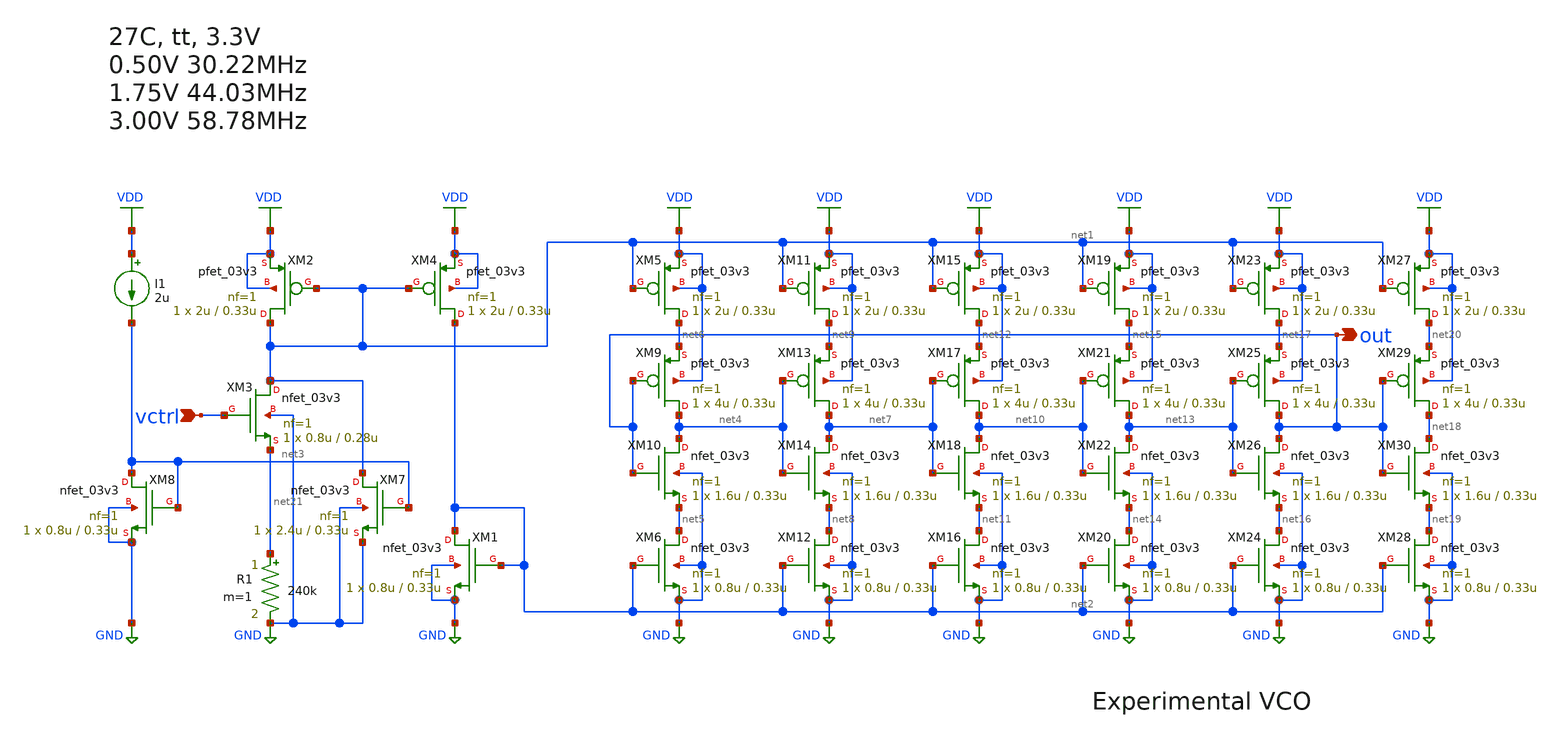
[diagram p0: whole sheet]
** sch_path: PLL/xschem/vco.sch
**.subckt vco vctrl out
*.ipin vctrl
*.opin out
XM2 net1 net1 VDD VDD pfet_03v3 L=0.33u W=2u nf=1 ad='int((nf+1)/2) * W/nf * 0.18u' as='int((nf+2)/2) * W/nf * 0.18u'
+ pd='2*int((nf+1)/2) * (W/nf + 0.18u)' ps='2*int((nf+2)/2) * (W/nf + 0.18u)' nrd='0.18u / W' nrs='0.18u / W'
+ sa=0 sb=0 sd=0 m=1
XM4 net2 net1 VDD VDD pfet_03v3 L=0.33u W=2u nf=1 ad='int((nf+1)/2) * W/nf * 0.18u' as='int((nf+2)/2) * W/nf * 0.18u'
+ pd='2*int((nf+1)/2) * (W/nf + 0.18u)' ps='2*int((nf+2)/2) * (W/nf + 0.18u)' nrd='0.18u / W' nrs='0.18u / W'
+ sa=0 sb=0 sd=0 m=1
XM1 net2 net2 GND GND nfet_03v3 L=0.33u W=0.8u nf=1 ad='int((nf+1)/2) * W/nf * 0.18u' as='int((nf+2)/2) * W/nf * 0.18u'
+ pd='2*int((nf+1)/2) * (W/nf + 0.18u)' ps='2*int((nf+2)/2) * (W/nf + 0.18u)' nrd='0.18u / W' nrs='0.18u / W'
+ sa=0 sb=0 sd=0 m=1
XM5 net6 net1 VDD VDD pfet_03v3 L=0.33u W=2u nf=1 ad='int((nf+1)/2) * W/nf * 0.18u' as='int((nf+2)/2) * W/nf * 0.18u'
+ pd='2*int((nf+1)/2) * (W/nf + 0.18u)' ps='2*int((nf+2)/2) * (W/nf + 0.18u)' nrd='0.18u / W' nrs='0.18u / W'
+ sa=0 sb=0 sd=0 m=1
XM6 net5 net2 GND GND nfet_03v3 L=0.33u W=0.8u nf=1 ad='int((nf+1)/2) * W/nf * 0.18u' as='int((nf+2)/2) * W/nf * 0.18u'
+ pd='2*int((nf+1)/2) * (W/nf + 0.18u)' ps='2*int((nf+2)/2) * (W/nf + 0.18u)' nrd='0.18u / W' nrs='0.18u / W'
+ sa=0 sb=0 sd=0 m=1
I1 VDD net3 2u
XM8 net3 net3 GND GND nfet_03v3 L=0.33u W=0.8u nf=1 ad='int((nf+1)/2) * W/nf * 0.18u' as='int((nf+2)/2) * W/nf * 0.18u'
+ pd='2*int((nf+1)/2) * (W/nf + 0.18u)' ps='2*int((nf+2)/2) * (W/nf + 0.18u)' nrd='0.18u / W' nrs='0.18u / W'
+ sa=0 sb=0 sd=0 m=1
R1 net21 GND 240k m=1
XM3 net1 vctrl net21 GND nfet_03v3 L=0.28u W=0.8u nf=1 ad='int((nf+1)/2) * W/nf * 0.18u' as='int((nf+2)/2) * W/nf * 0.18u'
+ pd='2*int((nf+1)/2) * (W/nf + 0.18u)' ps='2*int((nf+2)/2) * (W/nf + 0.18u)' nrd='0.18u / W' nrs='0.18u / W'
+ sa=0 sb=0 sd=0 m=1
XM7 net1 net3 GND GND nfet_03v3 L=0.33u W=2.4u nf=1 ad='int((nf+1)/2) * W/nf * 0.18u' as='int((nf+2)/2) * W/nf * 0.18u'
+ pd='2*int((nf+1)/2) * (W/nf + 0.18u)' ps='2*int((nf+2)/2) * (W/nf + 0.18u)' nrd='0.18u / W' nrs='0.18u / W'
+ sa=0 sb=0 sd=0 m=1
XM9 net4 out net6 VDD pfet_03v3 L=0.33u W=4u nf=1 ad='int((nf+1)/2) * W/nf * 0.18u' as='int((nf+2)/2) * W/nf * 0.18u'
+ pd='2*int((nf+1)/2) * (W/nf + 0.18u)' ps='2*int((nf+2)/2) * (W/nf + 0.18u)' nrd='0.18u / W' nrs='0.18u / W'
+ sa=0 sb=0 sd=0 m=1
XM10 net4 out net5 GND nfet_03v3 L=0.33u W=1.6u nf=1 ad='int((nf+1)/2) * W/nf * 0.18u' as='int((nf+2)/2) * W/nf * 0.18u'
+ pd='2*int((nf+1)/2) * (W/nf + 0.18u)' ps='2*int((nf+2)/2) * (W/nf + 0.18u)' nrd='0.18u / W' nrs='0.18u / W'
+ sa=0 sb=0 sd=0 m=1
XM11 net9 net1 VDD VDD pfet_03v3 L=0.33u W=2u nf=1 ad='int((nf+1)/2) * W/nf * 0.18u' as='int((nf+2)/2) * W/nf * 0.18u'
+ pd='2*int((nf+1)/2) * (W/nf + 0.18u)' ps='2*int((nf+2)/2) * (W/nf + 0.18u)' nrd='0.18u / W' nrs='0.18u / W'
+ sa=0 sb=0 sd=0 m=1
XM12 net8 net2 GND GND nfet_03v3 L=0.33u W=0.8u nf=1 ad='int((nf+1)/2) * W/nf * 0.18u' as='int((nf+2)/2) * W/nf * 0.18u'
+ pd='2*int((nf+1)/2) * (W/nf + 0.18u)' ps='2*int((nf+2)/2) * (W/nf + 0.18u)' nrd='0.18u / W' nrs='0.18u / W'
+ sa=0 sb=0 sd=0 m=1
XM13 net7 net4 net9 VDD pfet_03v3 L=0.33u W=4u nf=1 ad='int((nf+1)/2) * W/nf * 0.18u' as='int((nf+2)/2) * W/nf * 0.18u'
+ pd='2*int((nf+1)/2) * (W/nf + 0.18u)' ps='2*int((nf+2)/2) * (W/nf + 0.18u)' nrd='0.18u / W' nrs='0.18u / W'
+ sa=0 sb=0 sd=0 m=1
XM14 net7 net4 net8 GND nfet_03v3 L=0.33u W=1.6u nf=1 ad='int((nf+1)/2) * W/nf * 0.18u' as='int((nf+2)/2) * W/nf * 0.18u'
+ pd='2*int((nf+1)/2) * (W/nf + 0.18u)' ps='2*int((nf+2)/2) * (W/nf + 0.18u)' nrd='0.18u / W' nrs='0.18u / W'
+ sa=0 sb=0 sd=0 m=1
XM15 net12 net1 VDD VDD pfet_03v3 L=0.33u W=2u nf=1 ad='int((nf+1)/2) * W/nf * 0.18u' as='int((nf+2)/2) * W/nf * 0.18u'
+ pd='2*int((nf+1)/2) * (W/nf + 0.18u)' ps='2*int((nf+2)/2) * (W/nf + 0.18u)' nrd='0.18u / W' nrs='0.18u / W'
+ sa=0 sb=0 sd=0 m=1
XM16 net11 net2 GND GND nfet_03v3 L=0.33u W=0.8u nf=1 ad='int((nf+1)/2) * W/nf * 0.18u' as='int((nf+2)/2) * W/nf * 0.18u'
+ pd='2*int((nf+1)/2) * (W/nf + 0.18u)' ps='2*int((nf+2)/2) * (W/nf + 0.18u)' nrd='0.18u / W' nrs='0.18u / W'
+ sa=0 sb=0 sd=0 m=1
XM17 net10 net7 net12 VDD pfet_03v3 L=0.33u W=4u nf=1 ad='int((nf+1)/2) * W/nf * 0.18u' as='int((nf+2)/2) * W/nf * 0.18u'
+ pd='2*int((nf+1)/2) * (W/nf + 0.18u)' ps='2*int((nf+2)/2) * (W/nf + 0.18u)' nrd='0.18u / W' nrs='0.18u / W'
+ sa=0 sb=0 sd=0 m=1
XM18 net10 net7 net11 GND nfet_03v3 L=0.33u W=1.6u nf=1 ad='int((nf+1)/2) * W/nf * 0.18u' as='int((nf+2)/2) * W/nf * 0.18u'
+ pd='2*int((nf+1)/2) * (W/nf + 0.18u)' ps='2*int((nf+2)/2) * (W/nf + 0.18u)' nrd='0.18u / W' nrs='0.18u / W'
+ sa=0 sb=0 sd=0 m=1
XM19 net15 net1 VDD VDD pfet_03v3 L=0.33u W=2u nf=1 ad='int((nf+1)/2) * W/nf * 0.18u' as='int((nf+2)/2) * W/nf * 0.18u'
+ pd='2*int((nf+1)/2) * (W/nf + 0.18u)' ps='2*int((nf+2)/2) * (W/nf + 0.18u)' nrd='0.18u / W' nrs='0.18u / W'
+ sa=0 sb=0 sd=0 m=1
XM20 net14 net2 GND GND nfet_03v3 L=0.33u W=0.8u nf=1 ad='int((nf+1)/2) * W/nf * 0.18u' as='int((nf+2)/2) * W/nf * 0.18u'
+ pd='2*int((nf+1)/2) * (W/nf + 0.18u)' ps='2*int((nf+2)/2) * (W/nf + 0.18u)' nrd='0.18u / W' nrs='0.18u / W'
+ sa=0 sb=0 sd=0 m=1
XM21 net13 net10 net15 VDD pfet_03v3 L=0.33u W=4u nf=1 ad='int((nf+1)/2) * W/nf * 0.18u' as='int((nf+2)/2) * W/nf * 0.18u'
+ pd='2*int((nf+1)/2) * (W/nf + 0.18u)' ps='2*int((nf+2)/2) * (W/nf + 0.18u)' nrd='0.18u / W' nrs='0.18u / W'
+ sa=0 sb=0 sd=0 m=1
XM22 net13 net10 net14 GND nfet_03v3 L=0.33u W=1.6u nf=1 ad='int((nf+1)/2) * W/nf * 0.18u' as='int((nf+2)/2) * W/nf * 0.18u'
+ pd='2*int((nf+1)/2) * (W/nf + 0.18u)' ps='2*int((nf+2)/2) * (W/nf + 0.18u)' nrd='0.18u / W' nrs='0.18u / W'
+ sa=0 sb=0 sd=0 m=1
XM23 net17 net1 VDD VDD pfet_03v3 L=0.33u W=2u nf=1 ad='int((nf+1)/2) * W/nf * 0.18u' as='int((nf+2)/2) * W/nf * 0.18u'
+ pd='2*int((nf+1)/2) * (W/nf + 0.18u)' ps='2*int((nf+2)/2) * (W/nf + 0.18u)' nrd='0.18u / W' nrs='0.18u / W'
+ sa=0 sb=0 sd=0 m=1
XM24 net16 net2 GND GND nfet_03v3 L=0.33u W=0.8u nf=1 ad='int((nf+1)/2) * W/nf * 0.18u' as='int((nf+2)/2) * W/nf * 0.18u'
+ pd='2*int((nf+1)/2) * (W/nf + 0.18u)' ps='2*int((nf+2)/2) * (W/nf + 0.18u)' nrd='0.18u / W' nrs='0.18u / W'
+ sa=0 sb=0 sd=0 m=1
XM25 out net13 net17 VDD pfet_03v3 L=0.33u W=4u nf=1 ad='int((nf+1)/2) * W/nf * 0.18u' as='int((nf+2)/2) * W/nf * 0.18u'
+ pd='2*int((nf+1)/2) * (W/nf + 0.18u)' ps='2*int((nf+2)/2) * (W/nf + 0.18u)' nrd='0.18u / W' nrs='0.18u / W'
+ sa=0 sb=0 sd=0 m=1
XM26 out net13 net16 GND nfet_03v3 L=0.33u W=1.6u nf=1 ad='int((nf+1)/2) * W/nf * 0.18u' as='int((nf+2)/2) * W/nf * 0.18u'
+ pd='2*int((nf+1)/2) * (W/nf + 0.18u)' ps='2*int((nf+2)/2) * (W/nf + 0.18u)' nrd='0.18u / W' nrs='0.18u / W'
+ sa=0 sb=0 sd=0 m=1
XM27 net20 net1 VDD VDD pfet_03v3 L=0.33u W=2u nf=1 ad='int((nf+1)/2) * W/nf * 0.18u' as='int((nf+2)/2) * W/nf * 0.18u'
+ pd='2*int((nf+1)/2) * (W/nf + 0.18u)' ps='2*int((nf+2)/2) * (W/nf + 0.18u)' nrd='0.18u / W' nrs='0.18u / W'
+ sa=0 sb=0 sd=0 m=1
XM28 net19 net2 GND GND nfet_03v3 L=0.33u W=0.8u nf=1 ad='int((nf+1)/2) * W/nf * 0.18u' as='int((nf+2)/2) * W/nf * 0.18u'
+ pd='2*int((nf+1)/2) * (W/nf + 0.18u)' ps='2*int((nf+2)/2) * (W/nf + 0.18u)' nrd='0.18u / W' nrs='0.18u / W'
+ sa=0 sb=0 sd=0 m=1
XM29 net18 out net20 VDD pfet_03v3 L=0.33u W=4u nf=1 ad='int((nf+1)/2) * W/nf * 0.18u' as='int((nf+2)/2) * W/nf * 0.18u'
+ pd='2*int((nf+1)/2) * (W/nf + 0.18u)' ps='2*int((nf+2)/2) * (W/nf + 0.18u)' nrd='0.18u / W' nrs='0.18u / W'
+ sa=0 sb=0 sd=0 m=1
XM30 net18 out net19 GND nfet_03v3 L=0.33u W=1.6u nf=1 ad='int((nf+1)/2) * W/nf * 0.18u' as='int((nf+2)/2) * W/nf * 0.18u'
+ pd='2*int((nf+1)/2) * (W/nf + 0.18u)' ps='2*int((nf+2)/2) * (W/nf + 0.18u)' nrd='0.18u / W' nrs='0.18u / W'
+ sa=0 sb=0 sd=0 m=1
**.ends
.GLOBAL GND
.GLOBAL VDD
.end
